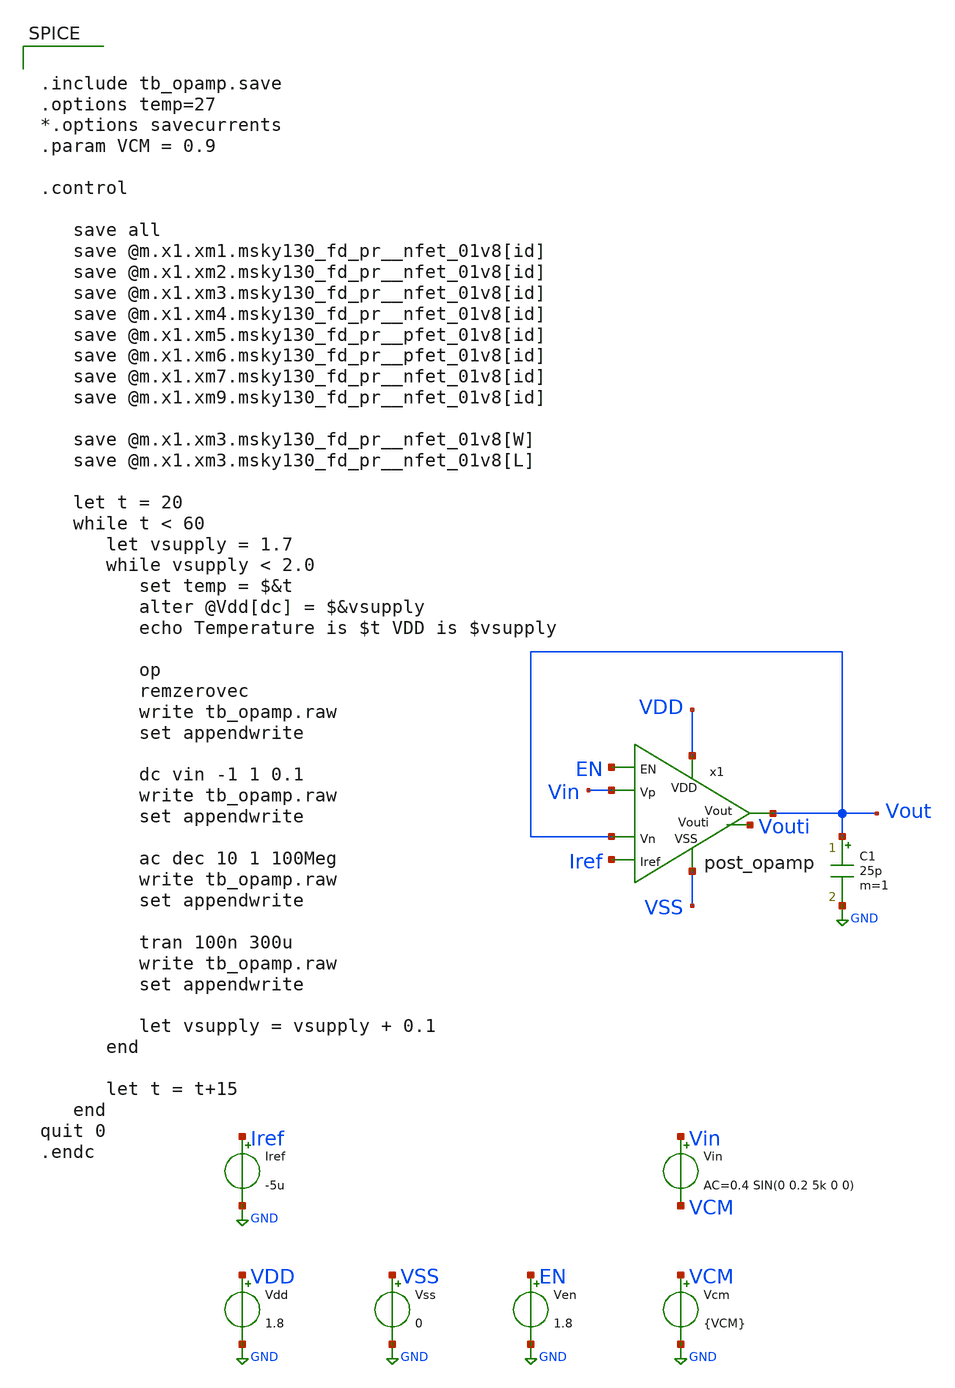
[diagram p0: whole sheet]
** sch_path: xschem/tb_post_closed_opamp.sch
**.subckt tb_post_closed_opamp
Vdd VDD GND 1.8
Vss VSS GND 0
Vin Vin VCM AC=0.4 SIN(0 0.2 5k 0 0)
Iref Iref GND -5u
Ven EN GND 1.8
C1 Vout GND 25p m=1
Vcm VCM GND {VCM}
x1 Vout Vout Vin VSS Iref VDD Vouti EN post_opamp
**** begin user architecture code


.include tb_opamp.save
.options temp=27
*.options savecurrents
.param VCM = 0.9

.control

   save all
   save @m.x1.xm1.msky130_fd_pr__nfet_01v8[id]
   save @m.x1.xm2.msky130_fd_pr__nfet_01v8[id]
   save @m.x1.xm3.msky130_fd_pr__nfet_01v8[id]
   save @m.x1.xm4.msky130_fd_pr__nfet_01v8[id]
   save @m.x1.xm5.msky130_fd_pr__pfet_01v8[id]
   save @m.x1.xm6.msky130_fd_pr__pfet_01v8[id]
   save @m.x1.xm7.msky130_fd_pr__nfet_01v8[id]
   save @m.x1.xm9.msky130_fd_pr__nfet_01v8[id]

   save @m.x1.xm3.msky130_fd_pr__nfet_01v8[W]
   save @m.x1.xm3.msky130_fd_pr__nfet_01v8[L]

   let t = 20
   while t < 60
      let vsupply = 1.7
      while vsupply < 2.0
         set temp = $&t
         alter @Vdd[dc] = $&vsupply
         echo Temperature is $t VDD is $vsupply

         op
         remzerovec
         write tb_opamp.raw
         set appendwrite

         dc vin -1 1 0.1
         write tb_opamp.raw
         set appendwrite

         ac dec 10 1 100Meg
         write tb_opamp.raw
         set appendwrite

         tran 100n 300u
         write tb_opamp.raw
         set appendwrite

         let vsupply = vsupply + 0.1
      end

      let t = t+15
   end
quit 0
.endc



** opencircuitdesign pdks install
.param MT_SWITCH = 1.0
.lib $::SKYWATER_MODELS/sky130.lib.spice tt

**** end user architecture code
**.ends
.GLOBAL GND
.end
